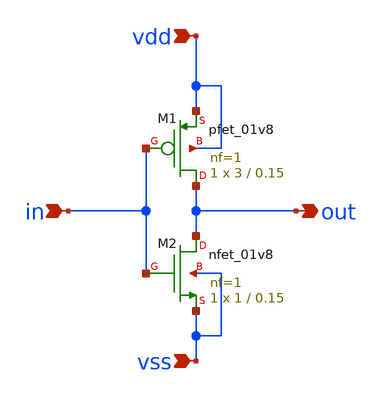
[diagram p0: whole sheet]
** sch_path: projects/carry_lookahead_adder/xschem/ports/inverter.sch
**.subckt inverter in vdd vss out
*.ipin in
*.ipin vdd
*.ipin vss
*.opin out
XM2 out in vss vss sky130_fd_pr__nfet_01v8 L=0.15 W=1 nf=1 ad='W * 0.29' as='W * 0.29' pd='W + 2 * 0.29'
+ ps='W + 2 * 0.29' nrd=0 nrs=0 sa=0 sb=0 sd=0 mult=1 m=1
XM1 out in vdd vdd sky130_fd_pr__pfet_01v8 L=0.15 W=3 nf=1 ad='W * 0.29' as='W * 0.29' pd='W + 2 * 0.29'
+ ps='W + 2 * 0.29' nrd=0 nrs=0 sa=0 sb=0 sd=0 mult=1 m=1
**.ends
.end
